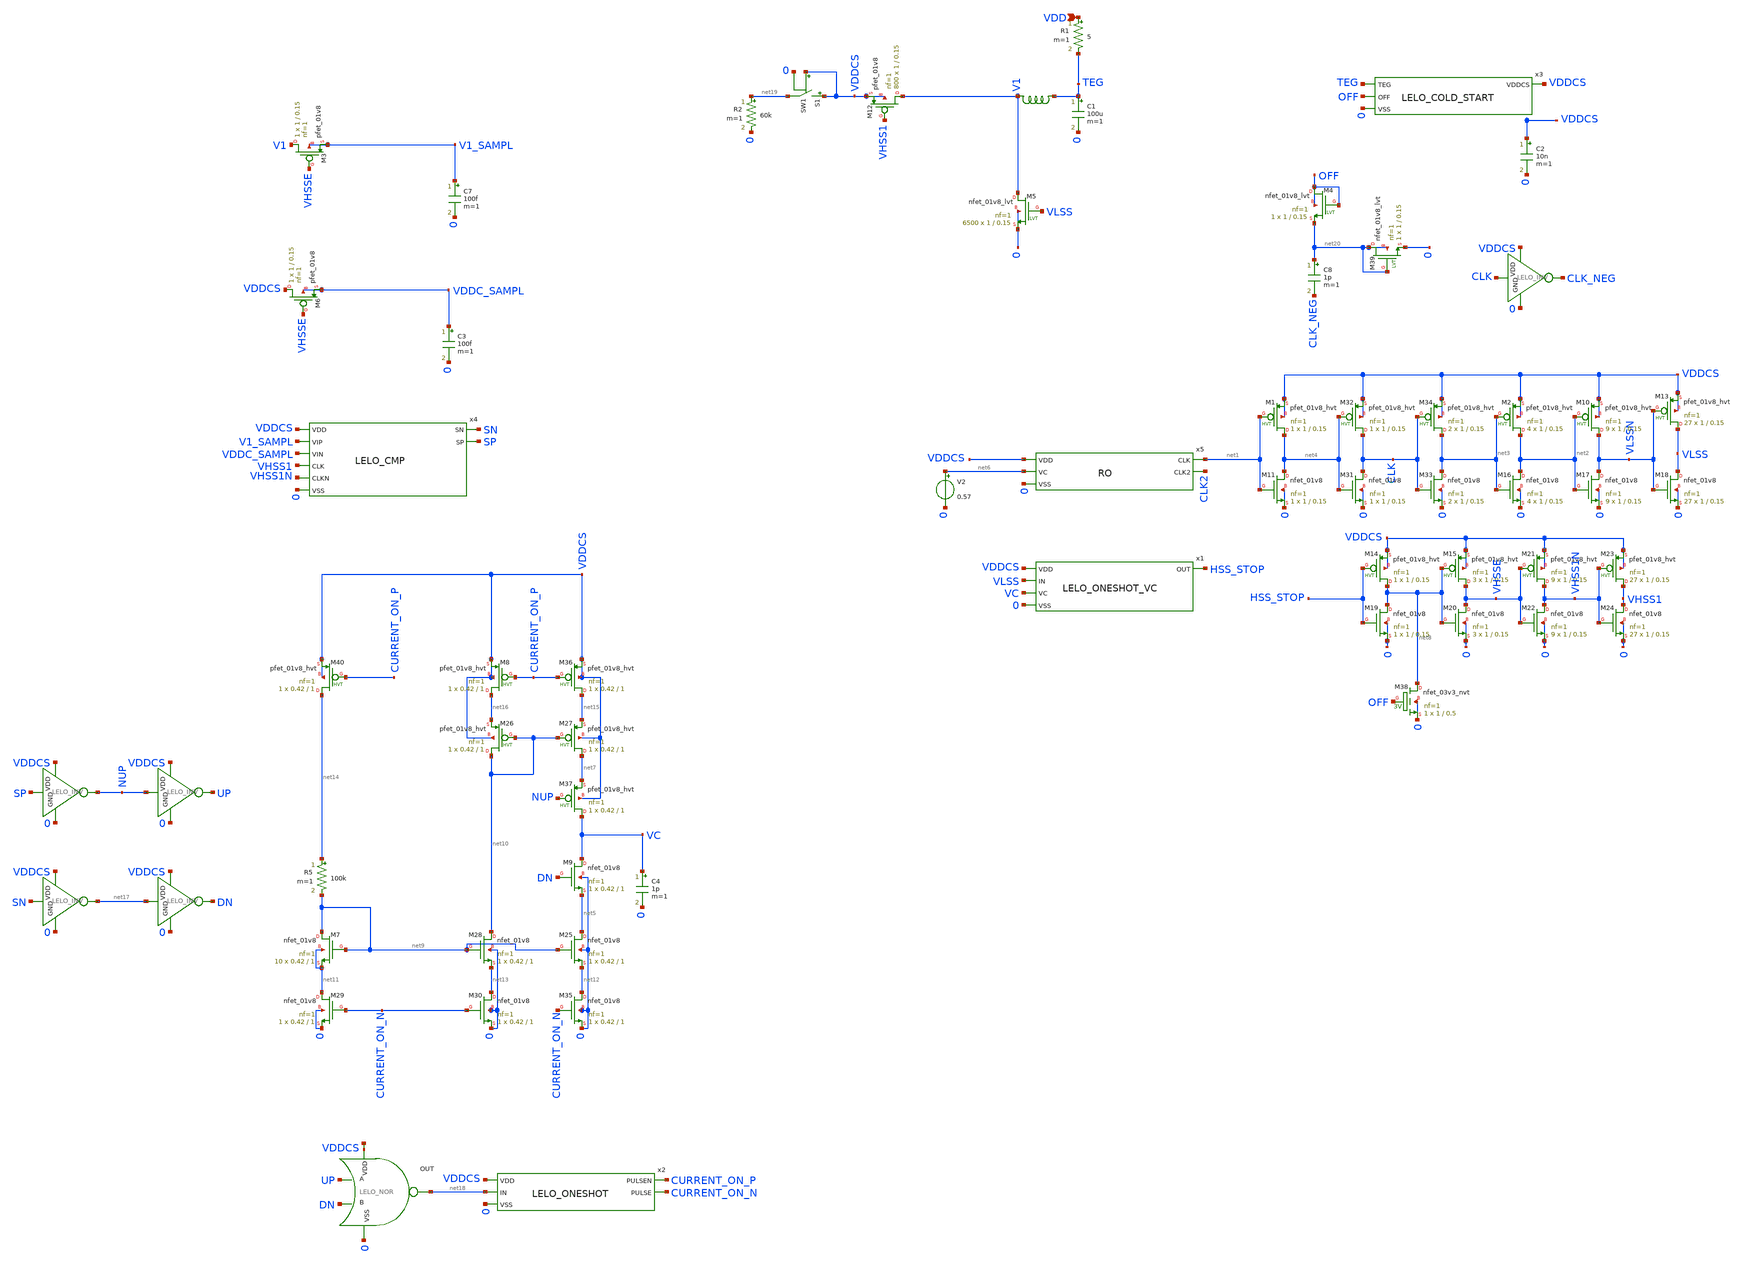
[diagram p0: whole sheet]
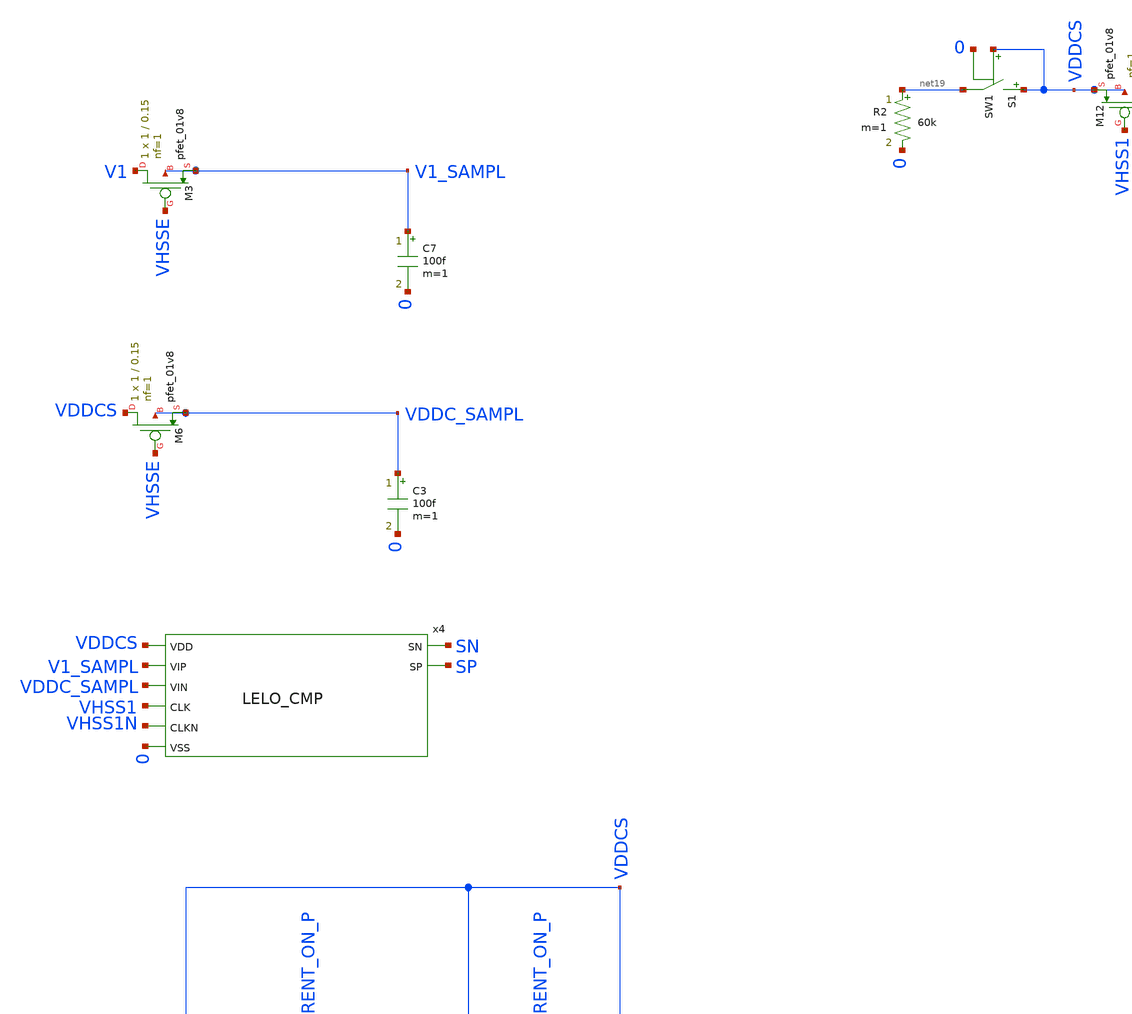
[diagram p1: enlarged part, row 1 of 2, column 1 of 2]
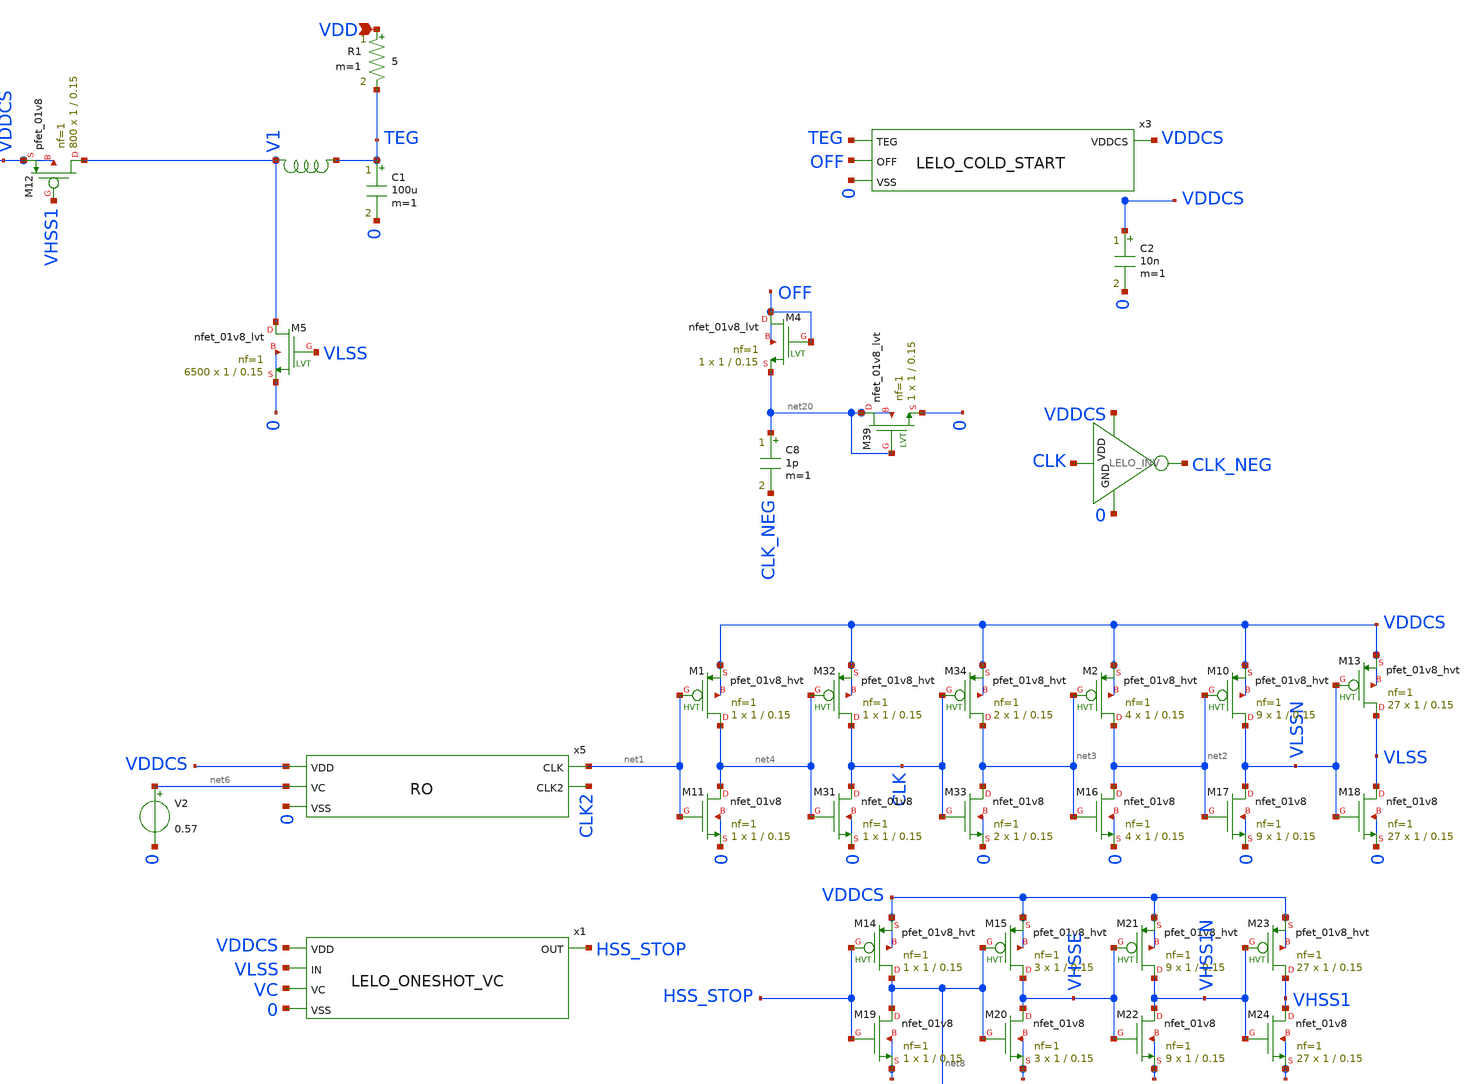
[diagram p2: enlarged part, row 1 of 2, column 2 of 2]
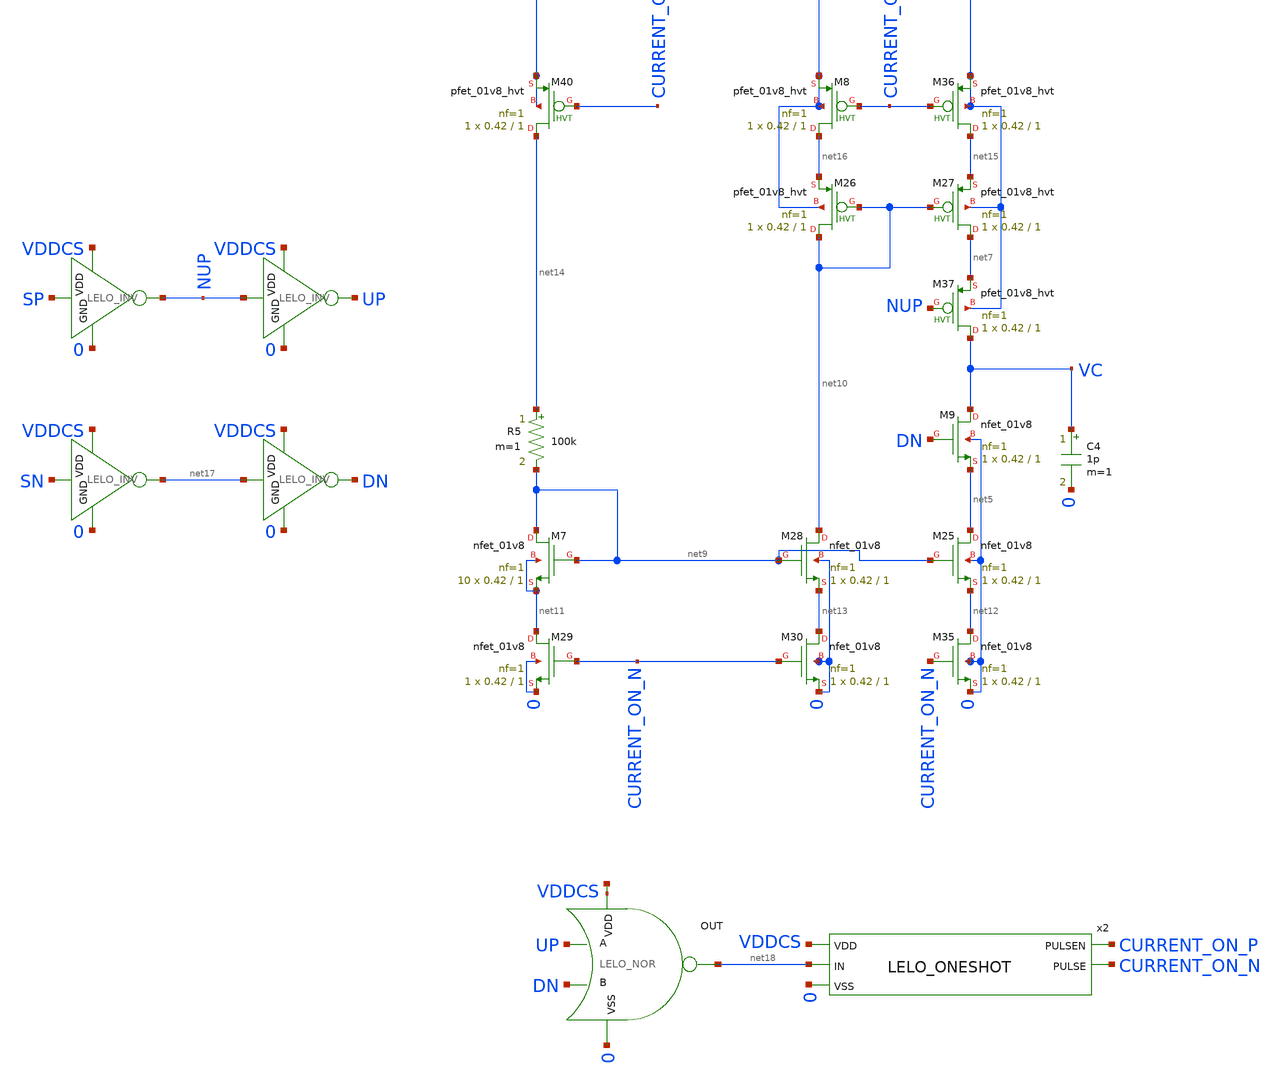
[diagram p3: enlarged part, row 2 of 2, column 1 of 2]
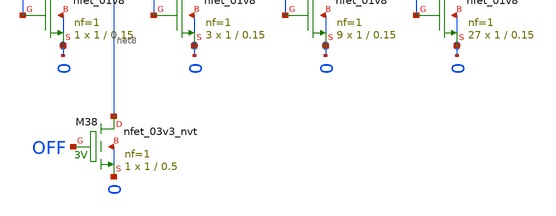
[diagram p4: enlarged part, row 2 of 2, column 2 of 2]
** sch_path: design/LELO_SVOD_SKY130A/LELO_EXSC.sch
**.subckt LELO_EXSC VDD
*.ipin VDD
R1 VDD TEG 5 m=1
C7 V1_SAMPL 0 100f m=1
x5 net1 CLK2 VDDCS net6 0 RO
XM12 V1 VHSS1 VDDCS VDDCS sky130_fd_pr__pfet_01v8 L=0.15 W=1 nf=1 ad='int((1 + 1)/2) * 1 / 1 * 0.29'
+ as='int((1 + 2)/2) * 1 / 1 * 0.29' pd='2*int((1 + 1)/2) * (1 / 1 + 0.29)' ps='2*int((1 + 2)/2) * (1 / 1 + 0.29)'
+ nrd='0.29 / 1 ' nrs='0.29 / 1 ' sa=0 sb=0 sd=0 mult=800 m=800
C1 TEG 0 100u m=1
XM5 V1 VLSS 0 0 sky130_fd_pr__nfet_01v8_lvt L=0.15 W=1 nf=1 ad='int((1 + 1)/2) * 1 / 1 * 0.29' as='int((1 + 2)/2) * 1 / 1 * 0.29'
+ pd='2*int((1 + 1)/2) * (1 / 1 + 0.29)' ps='2*int((1 + 2)/2) * (1 / 1 + 0.29)' nrd='0.29 / 1 ' nrs='0.29 / 1 '
+ sa=0 sb=0 sd=0 mult=6500 m=6500
x4 SN SP VDDCS V1_SAMPL VDDC_SAMPL VHSS1 VHSS1N 0 LELO_CMP
XM3 V1 VHSSE V1_SAMPL V1_SAMPL sky130_fd_pr__pfet_01v8 L=0.15 W=1 nf=1 ad='int((1 + 1)/2) * 1 / 1 * 0.29'
+ as='int((1 + 2)/2) * 1 / 1 * 0.29' pd='2*int((1 + 1)/2) * (1 / 1 + 0.29)' ps='2*int((1 + 2)/2) * (1 / 1 + 0.29)'
+ nrd='0.29 / 1 ' nrs='0.29 / 1 ' sa=0 sb=0 sd=0 mult=1 m=1
C3 VDDC_SAMPL 0 100f m=1
XM6 VDDCS VHSSE VDDC_SAMPL VDDC_SAMPL sky130_fd_pr__pfet_01v8 L=0.15 W=1 nf=1 ad='int((1 + 1)/2) * 1 / 1 * 0.29'
+ as='int((1 + 2)/2) * 1 / 1 * 0.29' pd='2*int((1 + 1)/2) * (1 / 1 + 0.29)' ps='2*int((1 + 2)/2) * (1 / 1 + 0.29)'
+ nrd='0.29 / 1 ' nrs='0.29 / 1 ' sa=0 sb=0 sd=0 mult=1 m=1
C4 VC 0 1p m=1
XM9 VC DN net5 0 sky130_fd_pr__nfet_01v8 L=1 W=0.42 nf=1 ad='int((1 + 1)/2) * 0.42 / 1 * 0.29' as='int((1 + 2)/2) * 0.42 / 1 * 0.29'
+ pd='2*int((1 + 1)/2) * (0.42 / 1 + 0.29)' ps='2*int((1 + 2)/2) * (0.42 / 1 + 0.29)' nrd='0.29 / 0.42 '
+ nrs='0.29 / 0.42 ' sa=0 sb=0 sd=0 mult=1 m=1
V2 net6 0 0.57
XM11 net4 net1 0 0 sky130_fd_pr__nfet_01v8 L=0.15 W=1 nf=1 ad='int((1 + 1)/2) * 1 / 1 * 0.29' as='int((1 + 2)/2) * 1 / 1 * 0.29'
+ pd='2*int((1 + 1)/2) * (1 / 1 + 0.29)' ps='2*int((1 + 2)/2) * (1 / 1 + 0.29)' nrd='0.29 / 1 ' nrs='0.29 / 1 '
+ sa=0 sb=0 sd=0 mult=1 m=1
XM16 net2 net3 0 0 sky130_fd_pr__nfet_01v8 L=0.15 W=1 nf=1 ad='int((1 + 1)/2) * 1 / 1 * 0.29' as='int((1 + 2)/2) * 1 / 1 * 0.29'
+ pd='2*int((1 + 1)/2) * (1 / 1 + 0.29)' ps='2*int((1 + 2)/2) * (1 / 1 + 0.29)' nrd='0.29 / 1 ' nrs='0.29 / 1 '
+ sa=0 sb=0 sd=0 mult=4 m=4
XM17 VLSSN net2 0 0 sky130_fd_pr__nfet_01v8 L=0.15 W=1 nf=1 ad='int((1 + 1)/2) * 1 / 1 * 0.29' as='int((1 + 2)/2) * 1 / 1 * 0.29'
+ pd='2*int((1 + 1)/2) * (1 / 1 + 0.29)' ps='2*int((1 + 2)/2) * (1 / 1 + 0.29)' nrd='0.29 / 1 ' nrs='0.29 / 1 '
+ sa=0 sb=0 sd=0 mult=9 m=9
XM18 VLSS VLSSN 0 0 sky130_fd_pr__nfet_01v8 L=0.15 W=1 nf=1 ad='int((1 + 1)/2) * 1 / 1 * 0.29' as='int((1 + 2)/2) * 1 / 1 * 0.29'
+ pd='2*int((1 + 1)/2) * (1 / 1 + 0.29)' ps='2*int((1 + 2)/2) * (1 / 1 + 0.29)' nrd='0.29 / 1 ' nrs='0.29 / 1 '
+ sa=0 sb=0 sd=0 mult=27 m=27
XM19 net8 HSS_STOP 0 0 sky130_fd_pr__nfet_01v8 L=0.15 W=1 nf=1 ad='int((1 + 1)/2) * 1 / 1 * 0.29' as='int((1 + 2)/2) * 1 / 1 * 0.29'
+ pd='2*int((1 + 1)/2) * (1 / 1 + 0.29)' ps='2*int((1 + 2)/2) * (1 / 1 + 0.29)' nrd='0.29 / 1 ' nrs='0.29 / 1 '
+ sa=0 sb=0 sd=0 mult=1 m=1
XM20 VHSSE net8 0 0 sky130_fd_pr__nfet_01v8 L=0.15 W=1 nf=1 ad='int((1 + 1)/2) * 1 / 1 * 0.29' as='int((1 + 2)/2) * 1 / 1 * 0.29'
+ pd='2*int((1 + 1)/2) * (1 / 1 + 0.29)' ps='2*int((1 + 2)/2) * (1 / 1 + 0.29)' nrd='0.29 / 1 ' nrs='0.29 / 1 '
+ sa=0 sb=0 sd=0 mult=3 m=3
XM22 VHSS1N VHSSE 0 0 sky130_fd_pr__nfet_01v8 L=0.15 W=1 nf=1 ad='int((1 + 1)/2) * 1 / 1 * 0.29' as='int((1 + 2)/2) * 1 / 1 * 0.29'
+ pd='2*int((1 + 1)/2) * (1 / 1 + 0.29)' ps='2*int((1 + 2)/2) * (1 / 1 + 0.29)' nrd='0.29 / 1 ' nrs='0.29 / 1 '
+ sa=0 sb=0 sd=0 mult=9 m=9
XM24 VHSS1 VHSS1N 0 0 sky130_fd_pr__nfet_01v8 L=0.15 W=1 nf=1 ad='int((1 + 1)/2) * 1 / 1 * 0.29' as='int((1 + 2)/2) * 1 / 1 * 0.29'
+ pd='2*int((1 + 1)/2) * (1 / 1 + 0.29)' ps='2*int((1 + 2)/2) * (1 / 1 + 0.29)' nrd='0.29 / 1 ' nrs='0.29 / 1 '
+ sa=0 sb=0 sd=0 mult=27 m=27
XM1 net4 net1 VDDCS VDDCS sky130_fd_pr__pfet_01v8_hvt L=0.15 W=1 nf=1 ad='int((1 + 1)/2) * 1 / 1 * 0.29'
+ as='int((1 + 2)/2) * 1 / 1 * 0.29' pd='2*int((1 + 1)/2) * (1 / 1 + 0.29)' ps='2*int((1 + 2)/2) * (1 / 1 + 0.29)'
+ nrd='0.29 / 1 ' nrs='0.29 / 1 ' sa=0 sb=0 sd=0 mult=1 m=1
XM2 net2 net3 VDDCS VDDCS sky130_fd_pr__pfet_01v8_hvt L=0.15 W=1 nf=1 ad='int((1 + 1)/2) * 1 / 1 * 0.29'
+ as='int((1 + 2)/2) * 1 / 1 * 0.29' pd='2*int((1 + 1)/2) * (1 / 1 + 0.29)' ps='2*int((1 + 2)/2) * (1 / 1 + 0.29)'
+ nrd='0.29 / 1 ' nrs='0.29 / 1 ' sa=0 sb=0 sd=0 mult=4 m=4
XM10 VLSSN net2 VDDCS VDDCS sky130_fd_pr__pfet_01v8_hvt L=0.15 W=1 nf=1 ad='int((1 + 1)/2) * 1 / 1 * 0.29'
+ as='int((1 + 2)/2) * 1 / 1 * 0.29' pd='2*int((1 + 1)/2) * (1 / 1 + 0.29)' ps='2*int((1 + 2)/2) * (1 / 1 + 0.29)'
+ nrd='0.29 / 1 ' nrs='0.29 / 1 ' sa=0 sb=0 sd=0 mult=9 m=9
XM13 VLSS VLSSN VDDCS VDDCS sky130_fd_pr__pfet_01v8_hvt L=0.15 W=1 nf=1 ad='int((1 + 1)/2) * 1 / 1 * 0.29'
+ as='int((1 + 2)/2) * 1 / 1 * 0.29' pd='2*int((1 + 1)/2) * (1 / 1 + 0.29)' ps='2*int((1 + 2)/2) * (1 / 1 + 0.29)'
+ nrd='0.29 / 1 ' nrs='0.29 / 1 ' sa=0 sb=0 sd=0 mult=27 m=27
XM14 net8 HSS_STOP VDDCS VDDCS sky130_fd_pr__pfet_01v8_hvt L=0.15 W=1 nf=1 ad='int((1 + 1)/2) * 1 / 1 * 0.29'
+ as='int((1 + 2)/2) * 1 / 1 * 0.29' pd='2*int((1 + 1)/2) * (1 / 1 + 0.29)' ps='2*int((1 + 2)/2) * (1 / 1 + 0.29)'
+ nrd='0.29 / 1 ' nrs='0.29 / 1 ' sa=0 sb=0 sd=0 mult=1 m=1
XM15 VHSSE net8 VDDCS VDDCS sky130_fd_pr__pfet_01v8_hvt L=0.15 W=1 nf=1 ad='int((1 + 1)/2) * 1 / 1 * 0.29'
+ as='int((1 + 2)/2) * 1 / 1 * 0.29' pd='2*int((1 + 1)/2) * (1 / 1 + 0.29)' ps='2*int((1 + 2)/2) * (1 / 1 + 0.29)'
+ nrd='0.29 / 1 ' nrs='0.29 / 1 ' sa=0 sb=0 sd=0 mult=3 m=3
XM21 VHSS1N VHSSE VDDCS VDDCS sky130_fd_pr__pfet_01v8_hvt L=0.15 W=1 nf=1 ad='int((1 + 1)/2) * 1 / 1 * 0.29'
+ as='int((1 + 2)/2) * 1 / 1 * 0.29' pd='2*int((1 + 1)/2) * (1 / 1 + 0.29)' ps='2*int((1 + 2)/2) * (1 / 1 + 0.29)'
+ nrd='0.29 / 1 ' nrs='0.29 / 1 ' sa=0 sb=0 sd=0 mult=9 m=9
XM23 VHSS1 VHSS1N VDDCS VDDCS sky130_fd_pr__pfet_01v8_hvt L=0.15 W=1 nf=1 ad='int((1 + 1)/2) * 1 / 1 * 0.29'
+ as='int((1 + 2)/2) * 1 / 1 * 0.29' pd='2*int((1 + 1)/2) * (1 / 1 + 0.29)' ps='2*int((1 + 2)/2) * (1 / 1 + 0.29)'
+ nrd='0.29 / 1 ' nrs='0.29 / 1 ' sa=0 sb=0 sd=0 mult=27 m=27
XM31 CLK net4 0 0 sky130_fd_pr__nfet_01v8 L=0.15 W=1 nf=1 ad='int((1 + 1)/2) * 1 / 1 * 0.29' as='int((1 + 2)/2) * 1 / 1 * 0.29'
+ pd='2*int((1 + 1)/2) * (1 / 1 + 0.29)' ps='2*int((1 + 2)/2) * (1 / 1 + 0.29)' nrd='0.29 / 1 ' nrs='0.29 / 1 '
+ sa=0 sb=0 sd=0 mult=1 m=1
XM32 CLK net4 VDDCS VDDCS sky130_fd_pr__pfet_01v8_hvt L=0.15 W=1 nf=1 ad='int((1 + 1)/2) * 1 / 1 * 0.29'
+ as='int((1 + 2)/2) * 1 / 1 * 0.29' pd='2*int((1 + 1)/2) * (1 / 1 + 0.29)' ps='2*int((1 + 2)/2) * (1 / 1 + 0.29)'
+ nrd='0.29 / 1 ' nrs='0.29 / 1 ' sa=0 sb=0 sd=0 mult=1 m=1
XM33 net3 CLK 0 0 sky130_fd_pr__nfet_01v8 L=0.15 W=1 nf=1 ad='int((1 + 1)/2) * 1 / 1 * 0.29' as='int((1 + 2)/2) * 1 / 1 * 0.29'
+ pd='2*int((1 + 1)/2) * (1 / 1 + 0.29)' ps='2*int((1 + 2)/2) * (1 / 1 + 0.29)' nrd='0.29 / 1 ' nrs='0.29 / 1 '
+ sa=0 sb=0 sd=0 mult=2 m=2
XM34 net3 CLK VDDCS VDDCS sky130_fd_pr__pfet_01v8_hvt L=0.15 W=1 nf=1 ad='int((1 + 1)/2) * 1 / 1 * 0.29'
+ as='int((1 + 2)/2) * 1 / 1 * 0.29' pd='2*int((1 + 1)/2) * (1 / 1 + 0.29)' ps='2*int((1 + 2)/2) * (1 / 1 + 0.29)'
+ nrd='0.29 / 1 ' nrs='0.29 / 1 ' sa=0 sb=0 sd=0 mult=2 m=2
x7 TEG V1 XGL6030-822_sat
x10 VDDCS SP NUP 0 LELO_INV
R5 net14 net9 100k m=1
XM7 net9 net9 net11 net11 sky130_fd_pr__nfet_01v8 L=1 W=0.42 nf=1 ad='int((1 + 1)/2) * 0.42 / 1 * 0.29'
+ as='int((1 + 2)/2) * 0.42 / 1 * 0.29' pd='2*int((1 + 1)/2) * (0.42 / 1 + 0.29)' ps='2*int((1 + 2)/2) * (0.42 / 1 + 0.29)'
+ nrd='0.29 / 0.42 ' nrs='0.29 / 0.42 ' sa=0 sb=0 sd=0 mult=10 m=10
XM25 net5 net9 net12 0 sky130_fd_pr__nfet_01v8 L=1 W=0.42 nf=1 ad='int((1 + 1)/2) * 0.42 / 1 * 0.29'
+ as='int((1 + 2)/2) * 0.42 / 1 * 0.29' pd='2*int((1 + 1)/2) * (0.42 / 1 + 0.29)' ps='2*int((1 + 2)/2) * (0.42 / 1 + 0.29)'
+ nrd='0.29 / 0.42 ' nrs='0.29 / 0.42 ' sa=0 sb=0 sd=0 mult=1 m=1
XM28 net10 net9 net13 0 sky130_fd_pr__nfet_01v8 L=1 W=0.42 nf=1 ad='int((1 + 1)/2) * 0.42 / 1 * 0.29'
+ as='int((1 + 2)/2) * 0.42 / 1 * 0.29' pd='2*int((1 + 1)/2) * (0.42 / 1 + 0.29)' ps='2*int((1 + 2)/2) * (0.42 / 1 + 0.29)'
+ nrd='0.29 / 0.42 ' nrs='0.29 / 0.42 ' sa=0 sb=0 sd=0 mult=1 m=1
XM29 net11 CURRENT_ON_N 0 0 sky130_fd_pr__nfet_01v8 L=1 W=0.42 nf=1 ad='int((1 + 1)/2) * 0.42 / 1 * 0.29'
+ as='int((1 + 2)/2) * 0.42 / 1 * 0.29' pd='2*int((1 + 1)/2) * (0.42 / 1 + 0.29)' ps='2*int((1 + 2)/2) * (0.42 / 1 + 0.29)'
+ nrd='0.29 / 0.42 ' nrs='0.29 / 0.42 ' sa=0 sb=0 sd=0 mult=1 m=1
XM30 net13 CURRENT_ON_N 0 0 sky130_fd_pr__nfet_01v8 L=1 W=0.42 nf=1 ad='int((1 + 1)/2) * 0.42 / 1 * 0.29'
+ as='int((1 + 2)/2) * 0.42 / 1 * 0.29' pd='2*int((1 + 1)/2) * (0.42 / 1 + 0.29)' ps='2*int((1 + 2)/2) * (0.42 / 1 + 0.29)'
+ nrd='0.29 / 0.42 ' nrs='0.29 / 0.42 ' sa=0 sb=0 sd=0 mult=1 m=1
XM35 net12 CURRENT_ON_N 0 0 sky130_fd_pr__nfet_01v8 L=1 W=0.42 nf=1 ad='int((1 + 1)/2) * 0.42 / 1 * 0.29'
+ as='int((1 + 2)/2) * 0.42 / 1 * 0.29' pd='2*int((1 + 1)/2) * (0.42 / 1 + 0.29)' ps='2*int((1 + 2)/2) * (0.42 / 1 + 0.29)'
+ nrd='0.29 / 0.42 ' nrs='0.29 / 0.42 ' sa=0 sb=0 sd=0 mult=1 m=1
x11 VDDCS SN net17 0 LELO_INV
x14 VDDCS net17 DN 0 LELO_INV
x15 net21 net18 UP DN 0 LELO_NOR
x17 VDDCS NUP UP 0 LELO_INV
XM40 net14 CURRENT_ON_P VDDCS VDDCS sky130_fd_pr__pfet_01v8_hvt L=1 W=0.42 nf=1 ad='int((1 + 1)/2) * 0.42 / 1 * 0.29'
+ as='int((1 + 2)/2) * 0.42 / 1 * 0.29' pd='2*int((1 + 1)/2) * (0.42 / 1 + 0.29)' ps='2*int((1 + 2)/2) * (0.42 / 1 + 0.29)'
+ nrd='0.29 / 0.42 ' nrs='0.29 / 0.42 ' sa=0 sb=0 sd=0 mult=1 m=1
XM8 net16 CURRENT_ON_P VDDCS VDDCS sky130_fd_pr__pfet_01v8_hvt L=1 W=0.42 nf=1 ad='int((1 + 1)/2) * 0.42 / 1 * 0.29'
+ as='int((1 + 2)/2) * 0.42 / 1 * 0.29' pd='2*int((1 + 1)/2) * (0.42 / 1 + 0.29)' ps='2*int((1 + 2)/2) * (0.42 / 1 + 0.29)'
+ nrd='0.29 / 0.42 ' nrs='0.29 / 0.42 ' sa=0 sb=0 sd=0 mult=1 m=1
XM26 net10 net10 net16 VDDCS sky130_fd_pr__pfet_01v8_hvt L=1 W=0.42 nf=1 ad='int((1 + 1)/2) * 0.42 / 1 * 0.29'
+ as='int((1 + 2)/2) * 0.42 / 1 * 0.29' pd='2*int((1 + 1)/2) * (0.42 / 1 + 0.29)' ps='2*int((1 + 2)/2) * (0.42 / 1 + 0.29)'
+ nrd='0.29 / 0.42 ' nrs='0.29 / 0.42 ' sa=0 sb=0 sd=0 mult=1 m=1
XM27 net7 net10 net15 VDDCS sky130_fd_pr__pfet_01v8_hvt L=1 W=0.42 nf=1 ad='int((1 + 1)/2) * 0.42 / 1 * 0.29'
+ as='int((1 + 2)/2) * 0.42 / 1 * 0.29' pd='2*int((1 + 1)/2) * (0.42 / 1 + 0.29)' ps='2*int((1 + 2)/2) * (0.42 / 1 + 0.29)'
+ nrd='0.29 / 0.42 ' nrs='0.29 / 0.42 ' sa=0 sb=0 sd=0 mult=1 m=1
XM36 net15 CURRENT_ON_P VDDCS VDDCS sky130_fd_pr__pfet_01v8_hvt L=1 W=0.42 nf=1 ad='int((1 + 1)/2) * 0.42 / 1 * 0.29'
+ as='int((1 + 2)/2) * 0.42 / 1 * 0.29' pd='2*int((1 + 1)/2) * (0.42 / 1 + 0.29)' ps='2*int((1 + 2)/2) * (0.42 / 1 + 0.29)'
+ nrd='0.29 / 0.42 ' nrs='0.29 / 0.42 ' sa=0 sb=0 sd=0 mult=1 m=1
XM37 VC NUP net7 VDDCS sky130_fd_pr__pfet_01v8_hvt L=1 W=0.42 nf=1 ad='int((1 + 1)/2) * 0.42 / 1 * 0.29'
+ as='int((1 + 2)/2) * 0.42 / 1 * 0.29' pd='2*int((1 + 1)/2) * (0.42 / 1 + 0.29)' ps='2*int((1 + 2)/2) * (0.42 / 1 + 0.29)'
+ nrd='0.29 / 0.42 ' nrs='0.29 / 0.42 ' sa=0 sb=0 sd=0 mult=1 m=1
C2 VDDCS 0 10n m=1
x1 VDDCS VLSS VC HSS_STOP 0 LELO_ONESHOT_VC
x2 VDDCS net18 0 CURRENT_ON_P CURRENT_ON_N LELO_ONESHOT
x3 TEG VDDCS OFF 0 LELO_COLD_START
R2 net19 0 60k m=1
XM38 net8 OFF 0 0 sky130_fd_pr__nfet_03v3_nvt L=0.5 W=1 nf=1 ad='int((1 + 1)/2) * 1 / 1 * 0.29' as='int((1 + 2)/2) * 1 / 1 * 0.29'
+ pd='2*int((1 + 1)/2) * (1 / 1 + 0.29)' ps='2*int((1 + 2)/2) * (1 / 1 + 0.29)' nrd='0.29 / 1 ' nrs='0.29 / 1 '
+ sa=0 sb=0 sd=0 mult=1 m=1
S1 VDDCS net19 VDDCS 0 SW1
C8 net20 CLK_NEG 1p m=1
XM4 OFF OFF net20 OFF sky130_fd_pr__nfet_01v8_lvt L=0.15 W=1 nf=1 ad='int((1 + 1)/2) * 1 / 1 * 0.29'
+ as='int((1 + 2)/2) * 1 / 1 * 0.29' pd='2*int((1 + 1)/2) * (1 / 1 + 0.29)' ps='2*int((1 + 2)/2) * (1 / 1 + 0.29)'
+ nrd='0.29 / 1 ' nrs='0.29 / 1 ' sa=0 sb=0 sd=0 mult=1 m=1
x8 VDDCS CLK CLK_NEG 0 LELO_INV
XM39 net20 net20 0 net20 sky130_fd_pr__nfet_01v8_lvt L=0.15 W=1 nf=1 ad='int((1 + 1)/2) * 1 / 1 * 0.29'
+ as='int((1 + 2)/2) * 1 / 1 * 0.29' pd='2*int((1 + 1)/2) * (1 / 1 + 0.29)' ps='2*int((1 + 2)/2) * (1 / 1 + 0.29)'
+ nrd='0.29 / 1 ' nrs='0.29 / 1 ' sa=0 sb=0 sd=0 mult=1 m=1
**.ends
**** begin user architecture code
.MODEL SW1 SW   VT=1.4 VH=0.2  RON=0.01 ROFF=10G
**** end user architecture code
.end
